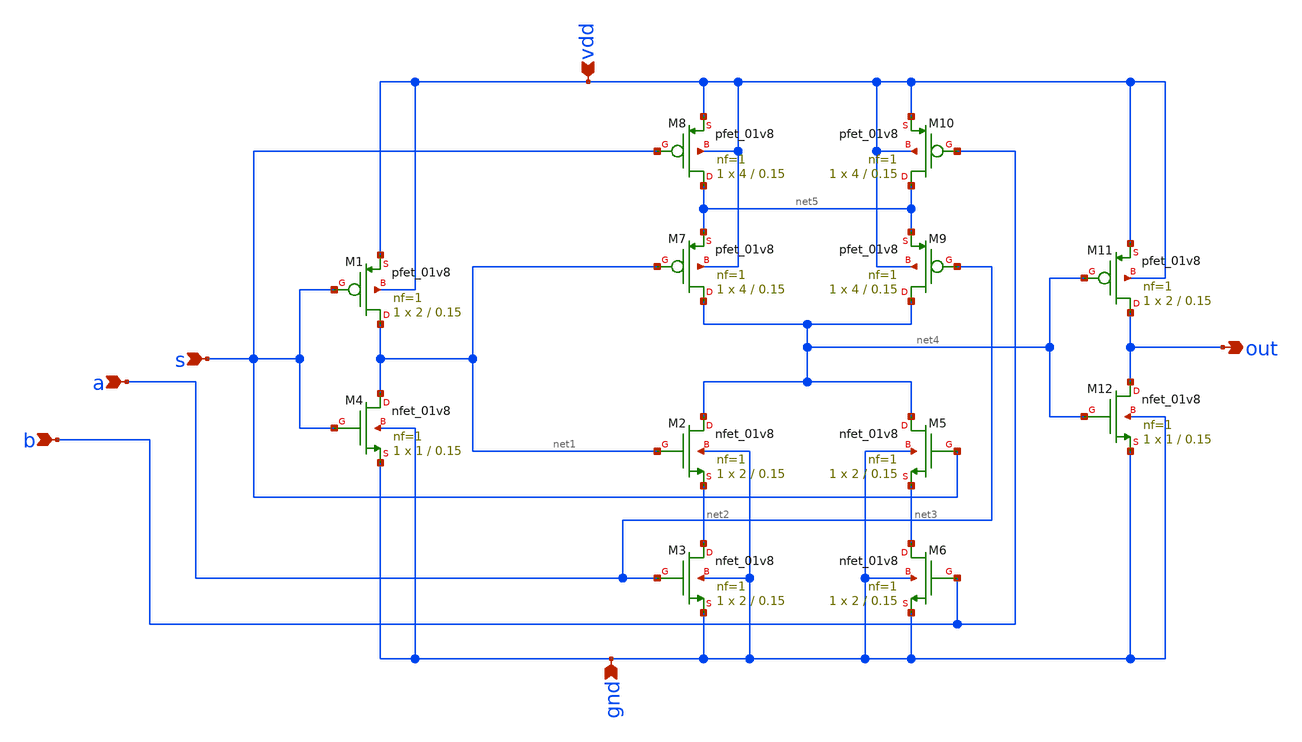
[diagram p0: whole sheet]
** sch_path: Projects/testfolder/two_one_mux.sch
**.subckt two_one_mux a b s vdd gnd out
*.ipin a
*.ipin b
*.ipin s
*.ipin vdd
*.ipin gnd
*.opin out
XM1 net1 s vdd vdd sky130_fd_pr__pfet_01v8 L=0.15 W=2 nf=1 ad='int((nf+1)/2) * W/nf * 0.29' as='int((nf+2)/2) * W/nf * 0.29'
+ pd='2*int((nf+1)/2) * (W/nf + 0.29)' ps='2*int((nf+2)/2) * (W/nf + 0.29)' nrd='0.29 / W' nrs='0.29 / W'
+ sa=0 sb=0 sd=0 mult=1 m=1
XM4 net1 s gnd gnd sky130_fd_pr__nfet_01v8 L=0.15 W=1 nf=1 ad='int((nf+1)/2) * W/nf * 0.29' as='int((nf+2)/2) * W/nf * 0.29'
+ pd='2*int((nf+1)/2) * (W/nf + 0.29)' ps='2*int((nf+2)/2) * (W/nf + 0.29)' nrd='0.29 / W' nrs='0.29 / W'
+ sa=0 sb=0 sd=0 mult=1 m=1
XM2 net4 net1 net2 gnd sky130_fd_pr__nfet_01v8 L=0.15 W=2 nf=1 ad='int((nf+1)/2) * W/nf * 0.29' as='int((nf+2)/2) * W/nf * 0.29'
+ pd='2*int((nf+1)/2) * (W/nf + 0.29)' ps='2*int((nf+2)/2) * (W/nf + 0.29)' nrd='0.29 / W' nrs='0.29 / W'
+ sa=0 sb=0 sd=0 mult=1 m=1
XM3 net2 a gnd gnd sky130_fd_pr__nfet_01v8 L=0.15 W=2 nf=1 ad='int((nf+1)/2) * W/nf * 0.29' as='int((nf+2)/2) * W/nf * 0.29'
+ pd='2*int((nf+1)/2) * (W/nf + 0.29)' ps='2*int((nf+2)/2) * (W/nf + 0.29)' nrd='0.29 / W' nrs='0.29 / W'
+ sa=0 sb=0 sd=0 mult=1 m=1
XM5 net4 s net3 gnd sky130_fd_pr__nfet_01v8 L=0.15 W=2 nf=1 ad='int((nf+1)/2) * W/nf * 0.29' as='int((nf+2)/2) * W/nf * 0.29'
+ pd='2*int((nf+1)/2) * (W/nf + 0.29)' ps='2*int((nf+2)/2) * (W/nf + 0.29)' nrd='0.29 / W' nrs='0.29 / W'
+ sa=0 sb=0 sd=0 mult=1 m=1
XM6 net3 b gnd gnd sky130_fd_pr__nfet_01v8 L=0.15 W=2 nf=1 ad='int((nf+1)/2) * W/nf * 0.29' as='int((nf+2)/2) * W/nf * 0.29'
+ pd='2*int((nf+1)/2) * (W/nf + 0.29)' ps='2*int((nf+2)/2) * (W/nf + 0.29)' nrd='0.29 / W' nrs='0.29 / W'
+ sa=0 sb=0 sd=0 mult=1 m=1
XM7 net4 net1 net5 vdd sky130_fd_pr__pfet_01v8 L=0.15 W=4 nf=1 ad='int((nf+1)/2) * W/nf * 0.29' as='int((nf+2)/2) * W/nf * 0.29'
+ pd='2*int((nf+1)/2) * (W/nf + 0.29)' ps='2*int((nf+2)/2) * (W/nf + 0.29)' nrd='0.29 / W' nrs='0.29 / W'
+ sa=0 sb=0 sd=0 mult=1 m=1
XM8 net5 s vdd vdd sky130_fd_pr__pfet_01v8 L=0.15 W=4 nf=1 ad='int((nf+1)/2) * W/nf * 0.29' as='int((nf+2)/2) * W/nf * 0.29'
+ pd='2*int((nf+1)/2) * (W/nf + 0.29)' ps='2*int((nf+2)/2) * (W/nf + 0.29)' nrd='0.29 / W' nrs='0.29 / W'
+ sa=0 sb=0 sd=0 mult=1 m=1
XM9 net4 a net5 vdd sky130_fd_pr__pfet_01v8 L=0.15 W=4 nf=1 ad='int((nf+1)/2) * W/nf * 0.29' as='int((nf+2)/2) * W/nf * 0.29'
+ pd='2*int((nf+1)/2) * (W/nf + 0.29)' ps='2*int((nf+2)/2) * (W/nf + 0.29)' nrd='0.29 / W' nrs='0.29 / W'
+ sa=0 sb=0 sd=0 mult=1 m=1
XM10 net5 b vdd vdd sky130_fd_pr__pfet_01v8 L=0.15 W=4 nf=1 ad='int((nf+1)/2) * W/nf * 0.29' as='int((nf+2)/2) * W/nf * 0.29'
+ pd='2*int((nf+1)/2) * (W/nf + 0.29)' ps='2*int((nf+2)/2) * (W/nf + 0.29)' nrd='0.29 / W' nrs='0.29 / W'
+ sa=0 sb=0 sd=0 mult=1 m=1
XM11 out net4 vdd vdd sky130_fd_pr__pfet_01v8 L=0.15 W=2 nf=1 ad='int((nf+1)/2) * W/nf * 0.29' as='int((nf+2)/2) * W/nf * 0.29'
+ pd='2*int((nf+1)/2) * (W/nf + 0.29)' ps='2*int((nf+2)/2) * (W/nf + 0.29)' nrd='0.29 / W' nrs='0.29 / W'
+ sa=0 sb=0 sd=0 mult=1 m=1
XM12 out net4 gnd gnd sky130_fd_pr__nfet_01v8 L=0.15 W=1 nf=1 ad='int((nf+1)/2) * W/nf * 0.29' as='int((nf+2)/2) * W/nf * 0.29'
+ pd='2*int((nf+1)/2) * (W/nf + 0.29)' ps='2*int((nf+2)/2) * (W/nf + 0.29)' nrd='0.29 / W' nrs='0.29 / W'
+ sa=0 sb=0 sd=0 mult=1 m=1
**.ends
.end
